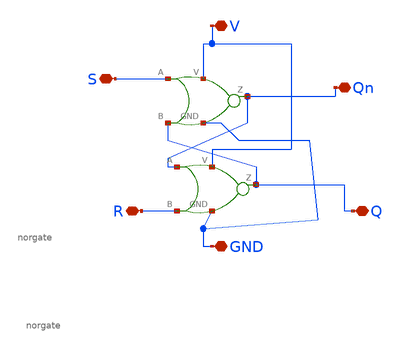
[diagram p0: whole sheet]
** sch_path: V2/Symbols/SR_nor.sch
**.subckt SR_nor V GND S R Qn Q
*.iopin V
*.iopin GND
*.iopin S
*.iopin R
*.iopin Qn
*.iopin Q
X1 S Q Qn GND V norgate
X1 Qn R Q GND V norgate
**** begin user architecture code

.include /foss/pdks/gf180mcuC/libs.tech/ngspice/design.ngspice
.lib /foss/pdks/gf180mcuC/libs.tech/ngspice/sm141064.ngspice typical

**** end user architecture code
**.ends
.end
